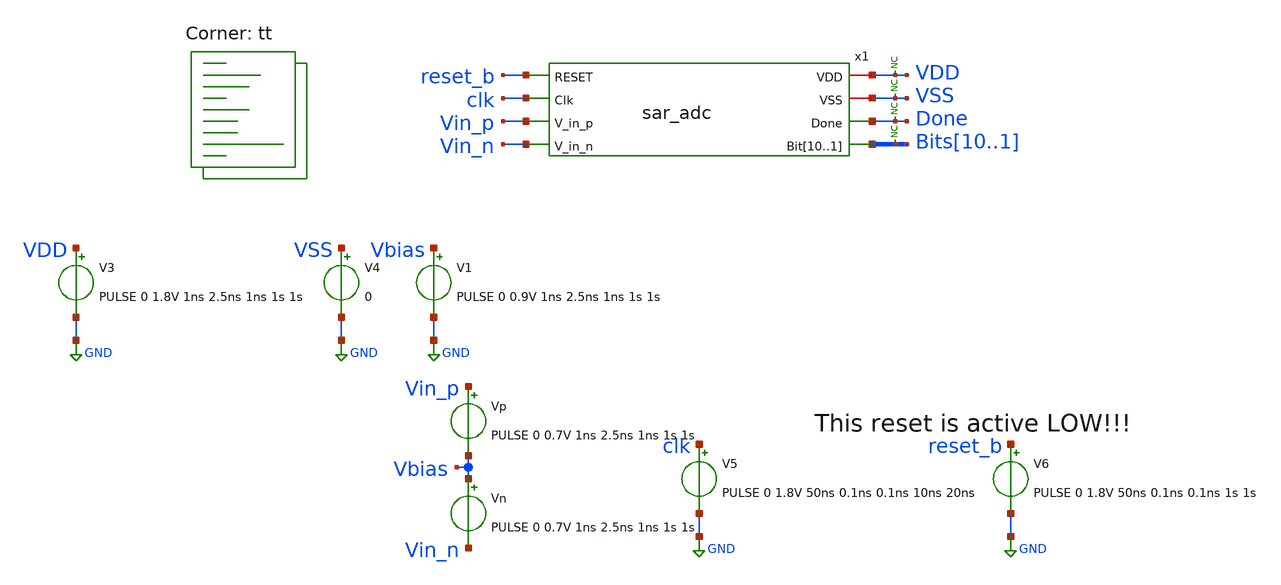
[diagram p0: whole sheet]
** sch_path: xschem/tests/sar_adc/sar_adc_code_step_max_sample_test.sch
**.subckt sar_adc_code_step_max_sample_test
V3 VDD GND PULSE 0 1.8V 1ns 2.5ns 1ns 1s 1s
V4 VSS GND 0
V1 Vbias GND PULSE 0 0.9V 1ns 2.5ns 1ns 1s 1s
* noconn VDD
* noconn VSS
* noconn Done
* noconn Bits[10..1]
Vn Vbias Vin_n PULSE 0 0.7V 1ns 2.5ns 1ns 1s 1s
V5 clk GND PULSE 0 1.8V 50ns 0.1ns 0.1ns 10ns 20ns
V6 reset_b GND PULSE 0 1.8V 50ns 0.1ns 0.1ns 1s 1s
Vp Vin_p Vbias PULSE 0 0.7V 1ns 2.5ns 1ns 1s 1s
x1 VDD VSS reset_b clk Vin_p Vin_n Done Bits10 Bits9 Bits8 Bits7 Bits6 Bits5 Bits4 Bits3 Bits2 Bits1
+ sar_adc
**** begin user architecture code

*.lib $::SKYWATER_MODELS/sky130.lib.spice tt

* .lib $::SKYWATER_MODELS/sky130.lib.spice.tt.red tt

.include $::SKYWATER_STDCELLS/sky130_fd_sc_hd.spice

.lib $::SKYWATER_MODELS/sky130.lib.spice tt



* Requires an iterator variable to be passed in!

* ngspice commands
.options list acct opts
.options method=gear
.control
save all
* Go to the const plot
setplot const

let diff_lsb = 1.8 / 1024
let diff_step = $&diff_lsb / 2
let steps_per_iter = 8
let iter_offset = $&steps_per_iter * diff_step

let vdiff = -0.9 + diff_step / 2 + $&iter_offset * $iterator
let vstart = $&vdiff
let vmax = $&vdiff + $&iter_offset
let vdelta = $&diff_step;

let total_runs = ceil(($&vmax - $&vdiff) / $&vdelta)
let runs = 0
let all_runs = $iterator * $&total_runs
let runs_start = $&runs

let out_bits = vector($&total_runs*10)
reshape out_bits[10][$&total_runs]
let in_diff_v= vector($&total_runs)
let vsampled_p = vector($&total_runs)
let vsampled_n = vector($&total_runs)

echo
echo AWS iterator = $iterator
echo vstart = $&vstart
echo vmax = $&vmax
echo vdiff = $&vdiff
echo diff_lsb = $&diff_lsb
echo diff_step = $&diff_step
echo steps_per_iter = $&steps_per_iter
echo iter_offset = $&iter_offset
echo total_runs = $&total_runs
echo runs = $&runs
echo

* Insert vector names and set only one scale
set wr_vecnames
set wr_singlescale

* set the hcopy type
set hcopydevtype=svg


while $&runs lt $&total_runs
	echo
	echo run = $&runs
	echo Vdiff = $&vdiff
	echo
	* Alter the voltages
	alter \@Vp[pulse] = [ 0 $&vdiff 1n 2.5n 1n 1 1 ] $ vector
	alter \@Vn[pulse] = [ 0 $&vdiff 1n 2.5n 1n 1 1 ] $ vector

	* Run the tran
	* tran creates a new plot starting with tran1
	tran 0.5n 700n uic

	set pltfile1 = plot_converg_{$&all_runs}_{$&vdiff}.svg
	set pltfile2 = plot_input_v_{$&all_runs}_{$&vdiff}.svg
	set pltfile3 = plot_clks_{$&all_runs}_{$&vdiff}.svg
	set pltfile4 = plot_raw_bits_{$&all_runs}_{$&vdiff}.svg
	set plttitle = run{$&all_runs}_vin{$&vdiff}
	hardcopy $pltfile1 x1.vsampled_p x1.vsampled_n x1.vsampled_p-x1.vsampled_n x1.sw_sample-2
+ x1.comp_out_p+2 x1.comp_out_n-2 title $plttitle
	*hardcopy $pltfile2 vin_p vin_n vss vdd vbias title $plttitle
	hardcopy $pltfile3 x1.x1.cycle0 x1.x1.cycle1 x1.x1.cycle2 x1.x1.cycle3 x1.x1.cycle4 x1.x1.cycle5
+ x1.x1.cycle6 x1.x1.cycle7 x1.x1.cycle8 x1.x1.cycle9 x1.x1.cycle10 x1.x1.cycle11 x1.x1.cycle12 x1.x1.cycle13
+ x1.x1.cycle14 x1.x1.cycle15 x1.controller_clk+2 title $plttitle
	hardcopy $pltfile4 x1.comp_out_p-2 x1.comp_out_n-4 x1.x1.raw_bit1 x1.x1.raw_bit2+2 x1.x1.raw_bit3+4
+ x1.x1.raw_bit4+6 x1.x1.raw_bit5+8 x1.x1.raw_bit6+10 x1.x1.raw_bit7+12 x1.x1.raw_bit8+14 x1.x1.raw_bit9+16
+ x1.x1.raw_bit10+18 x1.x1.raw_bit11+20 x1.x1.raw_bit12+22 x1.x1.raw_bit13+24 title $plttitle



	* Measure the max to find the output
	meas tran max_bit0 MAX v(bits1) from=650n to=655n
	meas tran max_bit1 MAX v(bits2) from=650n to=655n
	meas tran max_bit2 MAX v(bits3) from=650n to=655n
	meas tran max_bit3 MAX v(bits4) from=650n to=655n
	meas tran max_bit4 MAX v(bits5) from=650n to=655n
	meas tran max_bit5 MAX v(bits6) from=650n to=655n
	meas tran max_bit6 MAX v(bits7) from=650n to=655n
	meas tran max_bit7 MAX v(bits8) from=650n to=655n
	meas tran max_bit8 MAX v(bits9) from=650n to=655n
	meas tran max_bit9 MAX v(bits10) from=650n to=655n
	meas tran avg_vsampled_p AVG v(x1.vsampled_p) from=605n to=610n
	meas tran avg_vsampled_n AVG v(x1.vsampled_n) from=605n to=610n


	* Create variables
	set max_bit0 = $&max_bit0
	set max_bit1 = $&max_bit1
	set max_bit2 = $&max_bit2
	set max_bit3 = $&max_bit3
	set max_bit4 = $&max_bit4
	set max_bit5 = $&max_bit5
	set max_bit6 = $&max_bit6
	set max_bit7 = $&max_bit7
	set max_bit8 = $&max_bit8
	set max_bit9 = $&max_bit9
	set vdiff = $&vdiff
	set vsampled_p = $&avg_vsampled_p
	set vsampled_n = $&avg_vsampled_n

	* Switch to constants plot
	setplot const
	*compose out_bits values $&out_bits $p_max $n_max
	let in_diff_v[$&runs] = $vdiff
	let vsampled_p[$&runs] = $vsampled_p
	let vsampled_n[$&runs] = $vsampled_n
	let out_bits[0][$&runs] = $max_bit0
	let out_bits[1][$&runs] = $max_bit1
	let out_bits[2][$&runs] = $max_bit2
	let out_bits[3][$&runs] = $max_bit3
	let out_bits[4][$&runs] = $max_bit4
	let out_bits[5][$&runs] = $max_bit5
	let out_bits[6][$&runs] = $max_bit6
	let out_bits[7][$&runs] = $max_bit7
	let out_bits[8][$&runs] = $max_bit8
	let out_bits[9][$&runs] = $max_bit9

	* set the iterators
	echo run $&runs
	let vdiff = vdiff + vdelta
	let runs = runs + 1
	let all_runs = all_runs + 1

	* Destroy the transient plot to release memory
	destroy tran1

end

* switch to the const plot
setplot const
compose def_scale start=1 stop=$&total_runs step=1
setscale def_scale
echo Writing out_bits.txt
wrdata out_bits.txt vsampled_p vsampled_n in_diff_v out_bits

echo
echo Total Runs = $&runs
echo Run from = $&runs_start to = $&runs
echo Vdiff from = $&vstart to $&vdiff - $&vdelta
echo
.endc



**** end user architecture code
**.ends
.GLOBAL GND
.end
